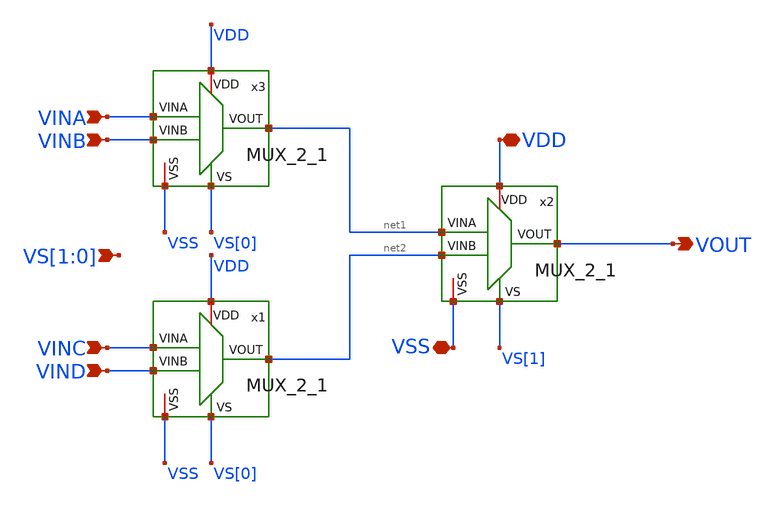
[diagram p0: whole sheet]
** sch_path: ADC8711-main/schematic/xschem/MUX_4_1.sch
**.subckt MUX_4_1 VOUT VDD VSS VINA VINB VINC VIND VS[1],VS[0]
*.opin VOUT
*.iopin VDD
*.iopin VSS
*.ipin VINA
*.ipin VINB
*.ipin VINC
*.ipin VIND
*.ipin VS[1],VS[0]
x3 VDD VINA net1 VS[0] VINB VSS MUX_2_1
x1 VDD VINC net2 VS[0] VIND VSS MUX_2_1
x2 VDD net1 VOUT VS[1] net2 VSS MUX_2_1
**.ends
.end
